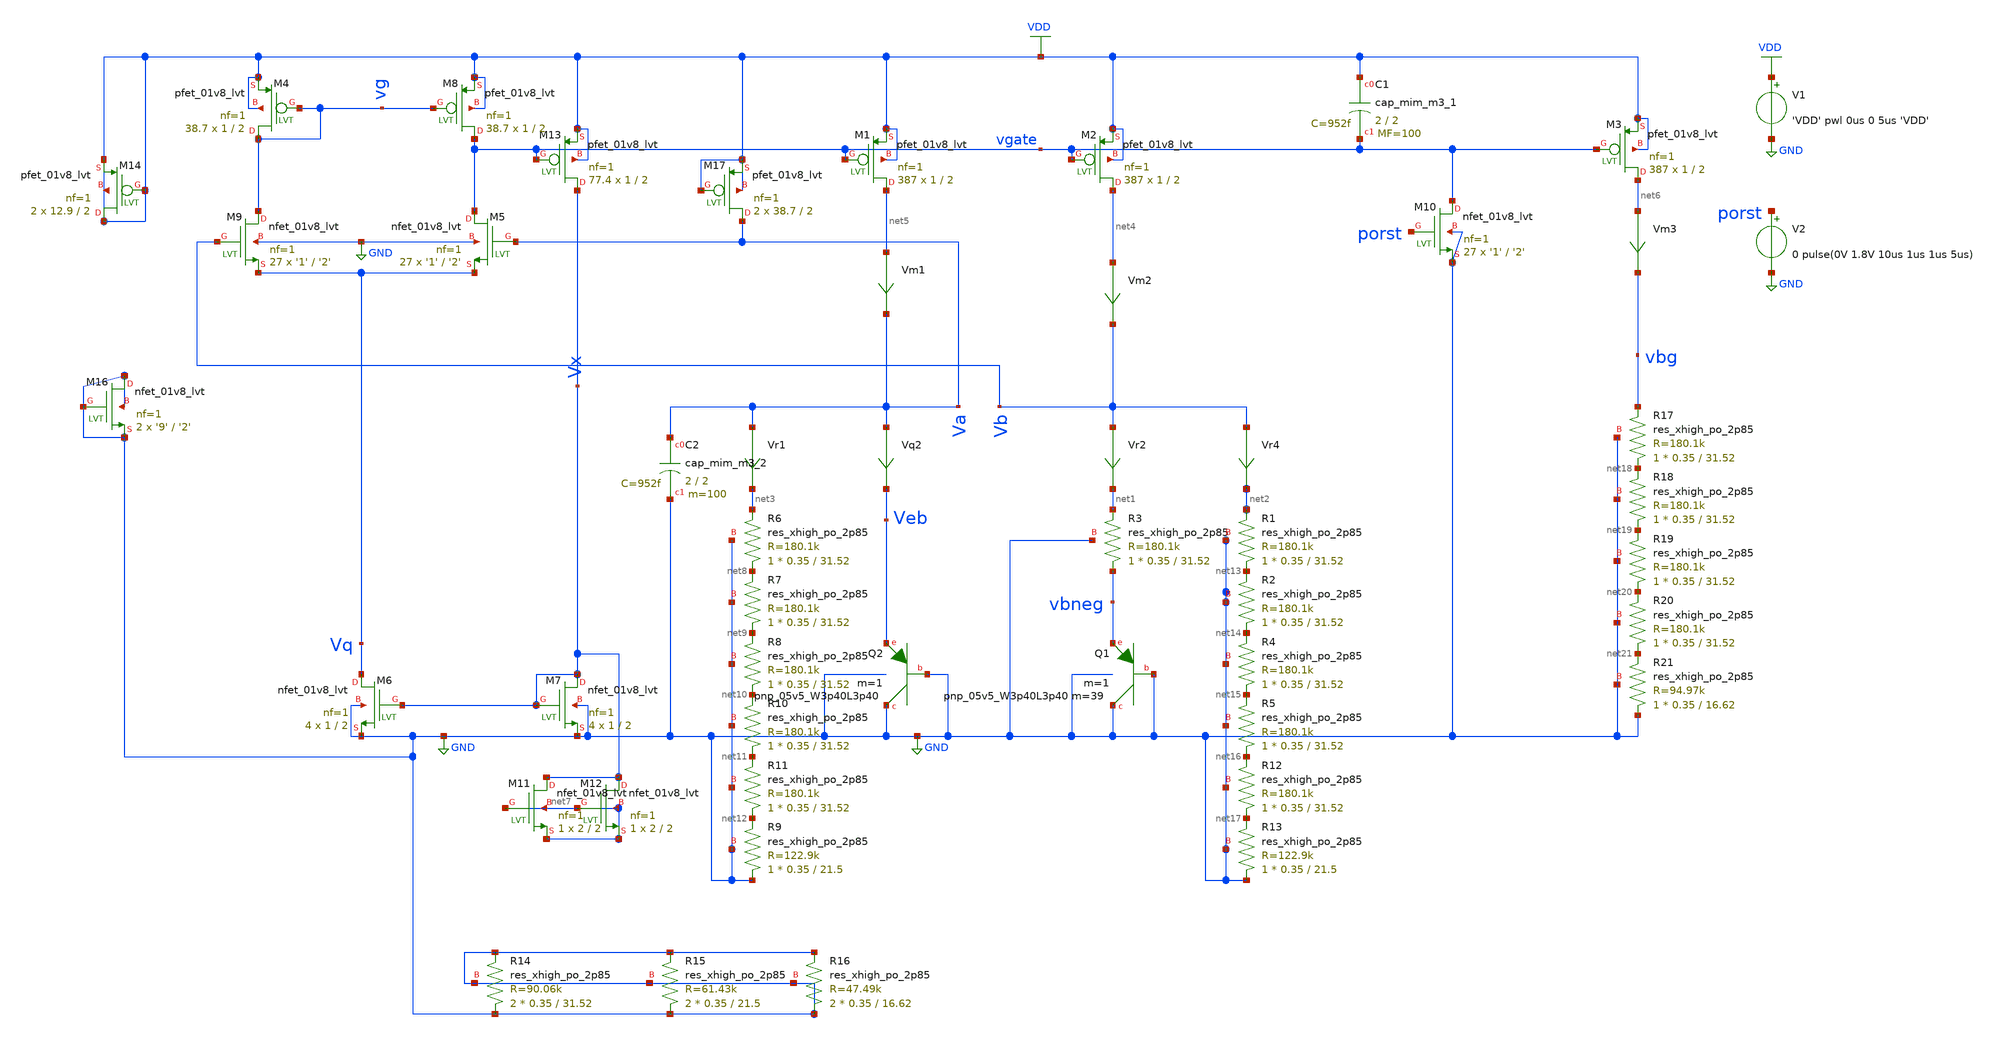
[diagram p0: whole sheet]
** sch_path: schematics/tsmc_bandgap_real_op_layout.sch
**.subckt tsmc_bandgap_real_op_layout
V1 VDD GND 'VDD' pwl 0us 0 5us 'VDD'
XQ2 GND GND Veb sky130_fd_pr__pnp_05v5_W3p40L3p40 m=1
Vr4 Vb net2 0
.save i(vr4)
Vr2 Vb net1 0
.save i(vr2)
Vm1 net5 Va 0
.save i(vm1)
Vm2 net4 Vb 0
.save i(vm2)
Vm3 net6 vbg 0
.save i(vm3)
Vr1 Va net3 0
.save i(vr1)
Vq2 Va Veb 0
.save i(vq2)
XQ1 GND GND vbneg sky130_fd_pr__pnp_05v5_W3p40L3p40 m=39 m=1
XM5 vgate Va Vq GND sky130_fd_pr__nfet_01v8_lvt L='2' W='1' nf=1 ad='int((nf+1)/2) * W/nf * 0.29' as='int((nf+2)/2) * W/nf * 0.29'
+ pd='2*int((nf+1)/2) * (W/nf + 0.29)' ps='2*int((nf+2)/2) * (W/nf + 0.29)' nrd='0.29 / W' nrs='0.29 / W'
+ sa=0 sb=0 sd=0 mult=27 m=27
XM6 Vq Vx GND GND sky130_fd_pr__nfet_01v8_lvt L=2 W=1 nf=1 ad='int((nf+1)/2) * W/nf * 0.29' as='int((nf+2)/2) * W/nf * 0.29'
+ pd='2*int((nf+1)/2) * (W/nf + 0.29)' ps='2*int((nf+2)/2) * (W/nf + 0.29)' nrd='0.29 / W' nrs='0.29 / W'
+ sa=0 sb=0 sd=0 mult=4 m=4
XM9 vg Vb Vq GND sky130_fd_pr__nfet_01v8_lvt L='2' W='1' nf=1 ad='int((nf+1)/2) * W/nf * 0.29' as='int((nf+2)/2) * W/nf * 0.29'
+ pd='2*int((nf+1)/2) * (W/nf + 0.29)' ps='2*int((nf+2)/2) * (W/nf + 0.29)' nrd='0.29 / W' nrs='0.29 / W'
+ sa=0 sb=0 sd=0 mult=27 m=27
XM7 Vx Vx GND GND sky130_fd_pr__nfet_01v8_lvt L=2 W=1 nf=1 ad='int((nf+1)/2) * W/nf * 0.29' as='int((nf+2)/2) * W/nf * 0.29'
+ pd='2*int((nf+1)/2) * (W/nf + 0.29)' ps='2*int((nf+2)/2) * (W/nf + 0.29)' nrd='0.29 / W' nrs='0.29 / W'
+ sa=0 sb=0 sd=0 mult=4 m=4
XM13 Vx vgate VDD VDD sky130_fd_pr__pfet_01v8_lvt L=2 W=1 nf=1 ad='int((nf+1)/2) * W/nf * 0.29' as='int((nf+2)/2) * W/nf * 0.29'
+ pd='2*int((nf+1)/2) * (W/nf + 0.29)' ps='2*int((nf+2)/2) * (W/nf + 0.29)' nrd='0.29 / W' nrs='0.29 / W'
+ sa=0 sb=0 sd=0 mult=77.4 m=77.4
XM1 net5 vgate VDD VDD sky130_fd_pr__pfet_01v8_lvt L=2 W=1 nf=1 ad='int((nf+1)/2) * W/nf * 0.29' as='int((nf+2)/2) * W/nf * 0.29'
+ pd='2*int((nf+1)/2) * (W/nf + 0.29)' ps='2*int((nf+2)/2) * (W/nf + 0.29)' nrd='0.29 / W' nrs='0.29 / W'
+ sa=0 sb=0 sd=0 mult=387 m=387
XM2 net4 vgate VDD VDD sky130_fd_pr__pfet_01v8_lvt L=2 W=1 nf=1 ad='int((nf+1)/2) * W/nf * 0.29' as='int((nf+2)/2) * W/nf * 0.29'
+ pd='2*int((nf+1)/2) * (W/nf + 0.29)' ps='2*int((nf+2)/2) * (W/nf + 0.29)' nrd='0.29 / W' nrs='0.29 / W'
+ sa=0 sb=0 sd=0 mult=387 m=387
XM3 net6 vgate VDD VDD sky130_fd_pr__pfet_01v8_lvt L=2 W=1 nf=1 ad='int((nf+1)/2) * W/nf * 0.29' as='int((nf+2)/2) * W/nf * 0.29'
+ pd='2*int((nf+1)/2) * (W/nf + 0.29)' ps='2*int((nf+2)/2) * (W/nf + 0.29)' nrd='0.29 / W' nrs='0.29 / W'
+ sa=0 sb=0 sd=0 mult=387 m=387
XM4 vg vg VDD VDD sky130_fd_pr__pfet_01v8_lvt L=2 W=1 nf=1 ad='int((nf+1)/2) * W/nf * 0.29' as='int((nf+2)/2) * W/nf * 0.29'
+ pd='2*int((nf+1)/2) * (W/nf + 0.29)' ps='2*int((nf+2)/2) * (W/nf + 0.29)' nrd='0.29 / W' nrs='0.29 / W'
+ sa=0 sb=0 sd=0 mult=38.7 m=38.7
XM8 vgate vg VDD VDD sky130_fd_pr__pfet_01v8_lvt L=2 W=1 nf=1 ad='int((nf+1)/2) * W/nf * 0.29' as='int((nf+2)/2) * W/nf * 0.29'
+ pd='2*int((nf+1)/2) * (W/nf + 0.29)' ps='2*int((nf+2)/2) * (W/nf + 0.29)' nrd='0.29 / W' nrs='0.29 / W'
+ sa=0 sb=0 sd=0 mult=38.7 m=38.7
XM10 vgate porst GND GND sky130_fd_pr__nfet_01v8_lvt L='2' W='1' nf=1 ad='int((nf+1)/2) * W/nf * 0.29'
+ as='int((nf+2)/2) * W/nf * 0.29' pd='2*int((nf+1)/2) * (W/nf + 0.29)' ps='2*int((nf+2)/2) * (W/nf + 0.29)'
+ nrd='0.29 / W' nrs='0.29 / W' sa=0 sb=0 sd=0 mult=27 m=27
V2 porst GND 0 pulse(0V 1.8V 10us 1us 1us 5us)
XR6 net8 net3 GND sky130_fd_pr__res_xhigh_po_2p85 L=31.52 mult=1 m=1
XR7 net9 net8 GND sky130_fd_pr__res_xhigh_po_2p85 L=31.52 mult=1 m=1
XR8 net10 net9 GND sky130_fd_pr__res_xhigh_po_2p85 L=31.52 mult=1 m=1
XR10 net11 net10 GND sky130_fd_pr__res_xhigh_po_2p85 L=31.52 mult=1 m=1
XR11 net12 net11 GND sky130_fd_pr__res_xhigh_po_2p85 L=31.52 mult=1 m=1
XR9 GND net12 GND sky130_fd_pr__res_xhigh_po_2p85 L=21.5 mult=1 m=1
XR3 vbneg net1 GND sky130_fd_pr__res_xhigh_po_2p85 L=31.52 mult=1 m=1
XR1 net13 net2 GND sky130_fd_pr__res_xhigh_po_2p85 L=31.52 mult=1 m=1
XR2 net14 net13 GND sky130_fd_pr__res_xhigh_po_2p85 L=31.52 mult=1 m=1
XR4 net15 net14 GND sky130_fd_pr__res_xhigh_po_2p85 L=31.52 mult=1 m=1
XR5 net16 net15 GND sky130_fd_pr__res_xhigh_po_2p85 L=31.52 mult=1 m=1
XR12 net17 net16 GND sky130_fd_pr__res_xhigh_po_2p85 L=31.52 mult=1 m=1
XR13 GND net17 GND sky130_fd_pr__res_xhigh_po_2p85 L=21.5 mult=1 m=1
XR17 net18 vbg GND sky130_fd_pr__res_xhigh_po_2p85 L=31.52 mult=1 m=1
XR18 net19 net18 GND sky130_fd_pr__res_xhigh_po_2p85 L=31.52 mult=1 m=1
XR19 net20 net19 GND sky130_fd_pr__res_xhigh_po_2p85 L=31.52 mult=1 m=1
XR20 net21 net20 GND sky130_fd_pr__res_xhigh_po_2p85 L=31.52 mult=1 m=1
XR21 GND net21 GND sky130_fd_pr__res_xhigh_po_2p85 L=16.62 mult=1 m=1
XC1 VDD vgate sky130_fd_pr__cap_mim_m3_1 W=2 L=2 MF=100 m=100
XC2 Va GND sky130_fd_pr__cap_mim_m3_2 W=2 L=2 MF=100 m=100
XR14 GND GND GND sky130_fd_pr__res_xhigh_po_2p85 L=31.52 mult=2 m=2
XR15 GND GND GND sky130_fd_pr__res_xhigh_po_2p85 L=21.5 mult=2 m=2
XR16 GND GND GND sky130_fd_pr__res_xhigh_po_2p85 L=16.62 mult=2 m=2
XM11 Vx net7 net7 net7 sky130_fd_pr__nfet_01v8_lvt L=2 W=2 nf=1 ad='int((nf+1)/2) * W/nf * 0.29' as='int((nf+2)/2) * W/nf * 0.29'
+ pd='2*int((nf+1)/2) * (W/nf + 0.29)' ps='2*int((nf+2)/2) * (W/nf + 0.29)' nrd='0.29 / W' nrs='0.29 / W'
+ sa=0 sb=0 sd=0 mult=1 m=1
XM12 Vx net7 net7 net7 sky130_fd_pr__nfet_01v8_lvt L=2 W=2 nf=1 ad='int((nf+1)/2) * W/nf * 0.29' as='int((nf+2)/2) * W/nf * 0.29'
+ pd='2*int((nf+1)/2) * (W/nf + 0.29)' ps='2*int((nf+2)/2) * (W/nf + 0.29)' nrd='0.29 / W' nrs='0.29 / W'
+ sa=0 sb=0 sd=0 mult=1 m=1
XM14 VDD VDD VDD VDD sky130_fd_pr__pfet_01v8_lvt L=2 W=12.9 nf=1 ad='int((nf+1)/2) * W/nf * 0.29' as='int((nf+2)/2) * W/nf * 0.29'
+ pd='2*int((nf+1)/2) * (W/nf + 0.29)' ps='2*int((nf+2)/2) * (W/nf + 0.29)' nrd='0.29 / W' nrs='0.29 / W'
+ sa=0 sb=0 sd=0 mult=2 m=2
XM16 GND GND GND GND sky130_fd_pr__nfet_01v8_lvt L='2' W='9' nf=1 ad='int((nf+1)/2) * W/nf * 0.29' as='int((nf+2)/2) * W/nf * 0.29'
+ pd='2*int((nf+1)/2) * (W/nf + 0.29)' ps='2*int((nf+2)/2) * (W/nf + 0.29)' nrd='0.29 / W' nrs='0.29 / W'
+ sa=0 sb=0 sd=0 mult=2 m=2
XM17 Va VDD VDD VDD sky130_fd_pr__pfet_01v8_lvt L=2 W=38.7 nf=1 ad='int((nf+1)/2) * W/nf * 0.29' as='int((nf+2)/2) * W/nf * 0.29'
+ pd='2*int((nf+1)/2) * (W/nf + 0.29)' ps='2*int((nf+2)/2) * (W/nf + 0.29)' nrd='0.29 / W' nrs='0.29 / W'
+ sa=0 sb=0 sd=0 mult=2 m=2
**** begin user architecture code

.include $::SKYWATER_MODELS/cells/nfet_01v8/sky130_fd_pr__nfet_01v8__tt.corner.spice
.include $::SKYWATER_MODELS/cells/nfet_01v8_lvt/sky130_fd_pr__nfet_01v8_lvt__tt.corner.spice
.include $::SKYWATER_MODELS/cells/pfet_01v8/sky130_fd_pr__pfet_01v8__tt.corner.spice
.include $::SKYWATER_MODELS/cells/nfet_03v3_nvt/sky130_fd_pr__nfet_03v3_nvt__tt.corner.spice
.include $::SKYWATER_MODELS/cells/nfet_05v0_nvt/sky130_fd_pr__nfet_05v0_nvt__tt.corner.spice
.include $::SKYWATER_MODELS/cells/esd_nfet_01v8/sky130_fd_pr__esd_nfet_01v8__tt.corner.spice
.include $::SKYWATER_MODELS/cells/pfet_01v8_lvt/sky130_fd_pr__pfet_01v8_lvt__tt.corner.spice
.include $::SKYWATER_MODELS/cells/pfet_01v8_hvt/sky130_fd_pr__pfet_01v8_hvt__tt.corner.spice
.include $::SKYWATER_MODELS/cells/esd_pfet_g5v0d10v5/sky130_fd_pr__esd_pfet_g5v0d10v5__tt.corner.spice
.include $::SKYWATER_MODELS/cells/pfet_g5v0d10v5/sky130_fd_pr__pfet_g5v0d10v5__tt.corner.spice
.include $::SKYWATER_MODELS/cells/pfet_g5v0d16v0/sky130_fd_pr__pfet_g5v0d16v0__tt.corner.spice
.include $::SKYWATER_MODELS/cells/nfet_g5v0d10v5/sky130_fd_pr__nfet_g5v0d10v5__tt.corner.spice
.include $::SKYWATER_MODELS/cells/nfet_g5v0d16v0/sky130_fd_pr__nfet_g5v0d16v0__tt_discrete.corner.spice
.include $::SKYWATER_MODELS/cells/esd_nfet_g5v0d10v5/sky130_fd_pr__esd_nfet_g5v0d10v5__tt.corner.spice
.include $::SKYWATER_MODELS/models/corners/tt/nonfet.spice
* Mismatch parameters
.include $::SKYWATER_MODELS/cells/nfet_01v8/sky130_fd_pr__nfet_01v8__mismatch.corner.spice
.include $::SKYWATER_MODELS/cells/pfet_01v8/sky130_fd_pr__pfet_01v8__mismatch.corner.spice
.include $::SKYWATER_MODELS/cells/nfet_01v8_lvt/sky130_fd_pr__nfet_01v8_lvt__mismatch.corner.spice
.include $::SKYWATER_MODELS/cells/pfet_01v8_lvt/sky130_fd_pr__pfet_01v8_lvt__mismatch.corner.spice
.include $::SKYWATER_MODELS/cells/pfet_01v8_hvt/sky130_fd_pr__pfet_01v8_hvt__mismatch.corner.spice
.include $::SKYWATER_MODELS/cells/nfet_g5v0d10v5/sky130_fd_pr__nfet_g5v0d10v5__mismatch.corner.spice
.include $::SKYWATER_MODELS/cells/pfet_g5v0d10v5/sky130_fd_pr__pfet_g5v0d10v5__mismatch.corner.spice
.include $::SKYWATER_MODELS/cells/nfet_05v0_nvt/sky130_fd_pr__nfet_05v0_nvt__mismatch.corner.spice
.include $::SKYWATER_MODELS/cells/nfet_03v3_nvt/sky130_fd_pr__nfet_03v3_nvt__mismatch.corner.spice
* Resistor$::SKYWATER_MODELS/Capacitor
.include $::SKYWATER_MODELS/models/r+c/res_typical__cap_typical.spice
.include $::SKYWATER_MODELS/models/r+c/res_typical__cap_typical__lin.spice
* Special cells
.include $::SKYWATER_MODELS/models/corners/tt/specialized_cells.spice
* All models
.include $::SKYWATER_MODELS/models/all.spice
*.include $::SKYWATER_MODELS/cells/pnp_05v5/sky130_fd_pr__pnp_05v5_W3p40L3p40.model.spice
.include /tmp/kustinj/ee272bclone/open_pdks/sky130A/libs.ref/sky130_fd_pr/spice/sky130_fd_pr__pnp_05v5_W3p40L3p40.model.spice
* Corner
.include $::SKYWATER_MODELS/models/corners/tt/rf.spice



.option savecurrents
.param mc_mm_switch=0
.param R3val='22.187k'
.param alpha='1'
.param R2R3ratio='5.6555038*alpha'
.param R2val='R3val*R2R3ratio'
.param R4R2ratio='0.79694273'
.param R4val='R2val*R4R2ratio
.param VDD=1.8
.nodeset v(vgate)=1.4

.control
save all  @m.xm1.msky130_fd_pr__pfet_01v8_lvt[gm]  @m.xm2.msky130_fd_pr__pfet_01v8_lvt[gm]  @m.xm3.msky130_fd_pr__pfet_01v8_lvt[gm]  @m.xm4.msky130_fd_pr__pfet_01v8_lvt[gm]  @m.xm5.msky130_fd_pr__nfet_01v8_lvt[gm]  @m.xm6.msky130_fd_pr__nfet_01v8_lvt[gm]  @m.xm7.msky130_fd_pr__nfet_01v8_lvt[gm]  @m.xm8.msky130_fd_pr__pfet_01v8_lvt[gm]  @m.xm9.msky130_fd_pr__nfet_01v8_lvt[gm]  @m.xm13.msky130_fd_pr__pfet_01v8_lvt[gm]

op
write tsmc_bandgap_real_op_layout.raw
let id8=@m.xm8.msky130_fd_pr__pfet_01v8_lvt[id]
let id1=@m.xm1.msky130_fd_pr__pfet_01v8_lvt[id]
let vth5=@m.xm5.msky130_fd_pr__nfet_01v8_lvt[vth]
let vth6=@m.xm6.msky130_fd_pr__nfet_01v8_lvt[vth]
let wm8=@m.xm8.msky130_fd_pr__pfet_01v8_lvt[w]
let mm8=@m.xm8.msky130_fd_pr__pfet_01v8_lvt[m]
let weff8=wm8*mm8
let jd8=id8/weff8
let wm1=@m.xm1.msky130_fd_pr__pfet_01v8_lvt[w]
let mm1=@m.xm1.msky130_fd_pr__pfet_01v8_lvt[m]
let weff1=wm1*mm1
let jd1=id1/weff1
let wm13=@m.xm13.msky130_fd_pr__pfet_01v8_lvt[w]
let mm13=@m.xm13.msky130_fd_pr__pfet_01v8_lvt[m]
let weff13=wm13*mm13
let id13=@m.xm13.msky130_fd_pr__pfet_01v8_lvt[id]
let jd13=id13/weff13
let gm13=@m.xm13.msky130_fd_pr__pfet_01v8_lvt[gm]
let gm3=@m.xm3.msky130_fd_pr__pfet_01v8_lvt[gm]
let gm4=@m.xm4.msky130_fd_pr__pfet_01v8_lvt[gm]
let gm5=@m.xm5.msky130_fd_pr__nfet_01v8_lvt[gm]
let gm6=@m.xm6.msky130_fd_pr__nfet_01v8_lvt[gm]
let gm7=@m.xm7.msky130_fd_pr__nfet_01v8_lvt[gm]
let gm8=@m.xm8.msky130_fd_pr__pfet_01v8_lvt[gm]
let gm9=@m.xm9.msky130_fd_pr__nfet_01v8_lvt[gm]
let gm1=@m.xm1.msky130_fd_pr__pfet_01v8_lvt[gm]
let gm2=@m.xm2.msky130_fd_pr__pfet_01v8_lvt[gm]
let vdsat1=2/(gm1/vm1#branch)
let vdsat2=2/(gm2/vm2#branch)
let vdsat3=2/(gm3/vm3#branch)
let vdsat4=2/(gm4/@m.xm4.msky130_fd_pr__pfet_01v8_lvt[id])
let vdsat5=2/(gm5/@m.xm5.msky130_fd_pr__nfet_01v8_lvt[id])
let vdsat6=2/(gm6/@m.xm6.msky130_fd_pr__nfet_01v8_lvt[id])
let vdsat7=2/(gm7/@m.xm7.msky130_fd_pr__nfet_01v8_lvt[id])
let vdsat8=2/(gm8/@m.xm8.msky130_fd_pr__pfet_01v8_lvt[id])
let vdsat9=2/(gm9/@m.xm9.msky130_fd_pr__nfet_01v8_lvt[id])
let vdsat13=2/(gm13/@m.xm13.msky130_fd_pr__pfet_01v8_lvt[id])


print vbg vgate vg va vb vx vq
print vdsat1 vdsat2 vdsat3 vdsat4   vdsat5 vdsat6 vdsat7 vdsat8 vdsat9 vdsat13
.endc


**** end user architecture code
**.ends
.GLOBAL VDD
.GLOBAL GND
.end
